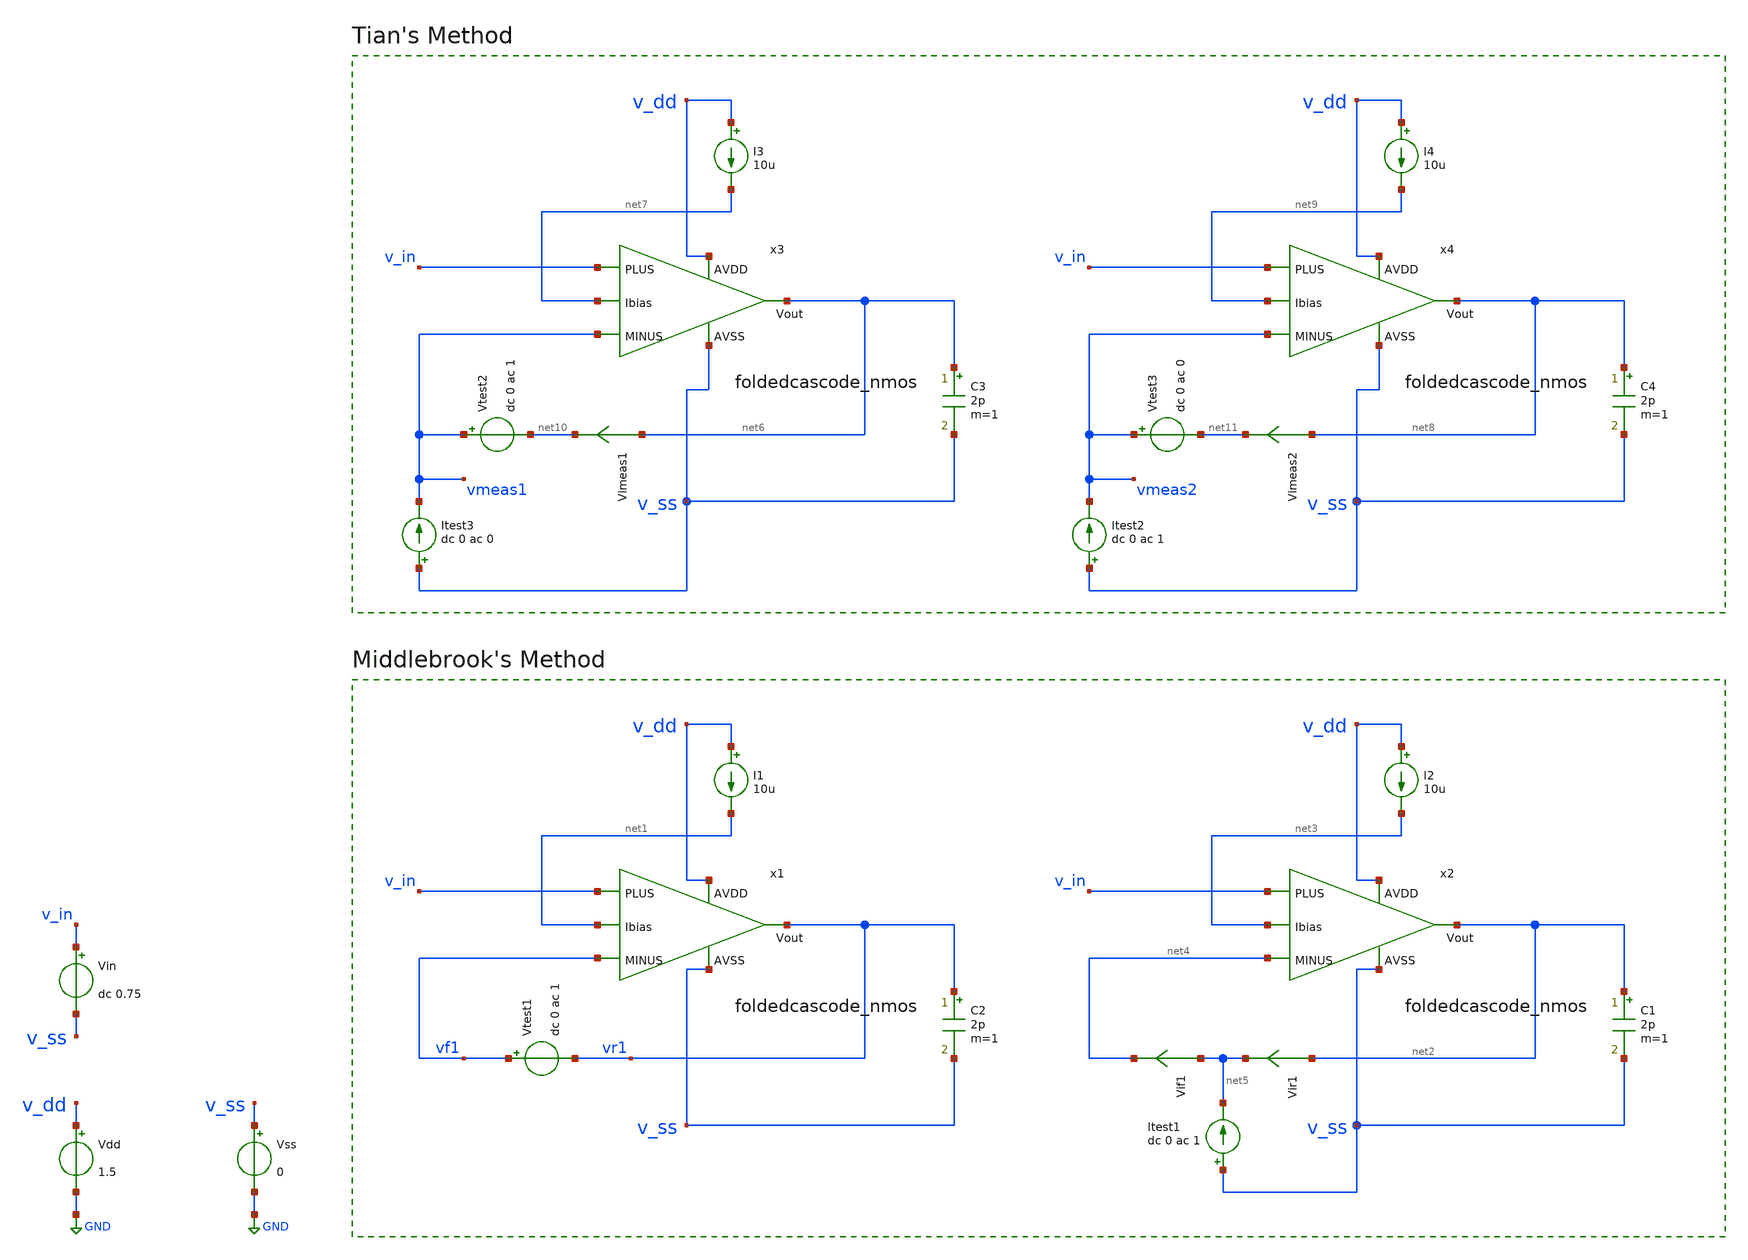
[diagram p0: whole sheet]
** sch_path: Designs/otas/1_schematics/tb_foldedcascode_nmos_loopgain.sch
* (c) 2025 Thesis_HP, Apache-2.0 license
**.subckt tb_foldedcascode_nmos_loopgain
Vdd v_dd GND 1.5
Vss v_ss GND 0
Vin v_in v_ss dc 0.75
C2 vr1 v_ss 2p m=1
I1 v_dd net1 10u
Vtest1 vf1 vr1 dc 0 ac 1
C1 net2 v_ss 2p m=1
I2 v_dd net3 10u
Vir1 net2 net5 0
.save i(vir1)
Vif1 net5 net4 0
.save i(vif1)
Itest1 v_ss net5 dc 0 ac 1
C3 net6 v_ss 2p m=1
I3 v_dd net7 10u
C4 net8 v_ss 2p m=1
I4 v_dd net9 10u
Itest3 v_ss vmeas1 dc 0 ac 0
Vtest2 vmeas1 net10 dc 0 ac 1
Vimeas1 net6 net10 0
.save i(vimeas1)
Itest2 v_ss vmeas2 dc 0 ac 1
Vtest3 vmeas2 net11 dc 0 ac 0
Vimeas2 net8 net11 0
.save i(vimeas2)
x3 v_dd v_in vmeas1 net6 net7 v_ss foldedcascode_nmos
x4 v_dd v_in vmeas2 net8 net9 v_ss foldedcascode_nmos
x1 v_dd v_in vf1 vr1 net1 v_ss foldedcascode_nmos
x2 v_dd v_in net4 net2 net3 v_ss foldedcascode_nmos
**** begin user architecture code

.lib cornerMOSlv.lib mos_tt
.lib cornerRES.lib res_typ



.param temp=27
.options savecurrents reltol=1e-3 abstol=1e-12 gmin=1e-15
.control
save all

* Operating Point Analysis
op
remzerovec
write foldedcascode_nmos_tb-loopgain.raw
set appendwrite

* AC Analysis
ac dec 101 1 100G
remzerovec
write foldedcascode_nmos_tb-loopgain.raw
set appendwrite

* Middlebrook's Method
let tv=-v(vr1)/v(vf1)
let ti=-i(vir1)/i(vif1)
let tmb=(tv*ti - 1)/(tv + ti + 2)

plot db(tmb) ylabel 'Magnitude - Middlebrook'
plot 180/pi*cphase(tmb) ylabel 'Phase - Middlebrook'

* Tian's Method
* vtest=0, itest=1:
let A=i(Vimeas2)
let C=v(vmeas2)

* vtest=1, itest=0:
let B=i(Vimeas1)
let D=v(vmeas1)
let ttian=(A*D-B*C-A)/(2*(B*C-A*D)+A-D+1)

plot db(ttian) ylabel 'Magnitude - Tian'
plot 180/pi*cphase(ttian) ylabel 'Phase - Tian'

* Middlebrook vs. Tian
plot db(tmb) db(ttian) ylabel 'Magnitude'
plot 180/pi*cphase(tmb) 180/pi*cphase(ttian) ylabel 'Phase'

write foldedcascode_nmos_tb-loopgain.raw

*quit
.endc


**** end user architecture code
**.ends

* expanding   symbol:  foldedcascode_nmos.sym # of pins=6
** sym_path: Designs/otas/foldedcascode_nmos.sym
** sch_path: Designs/otas/foldedcascode_nmos.sch
.subckt foldedcascode_nmos AVDD PLUS MINUS Vout Ibias AVSS
*.ipin PLUS
*.ipin MINUS
*.opin Vout
*.ipin AVDD
*.ipin AVSS
*.ipin Ibias
XM6 net5 PLUS net1 AVSS sg13_lv_nmos w=5u l=1u ng=1 m=1 mm_ok=1
XM8 net1 Ibias AVSS AVSS sg13_lv_nmos w=25u l=5u ng=3 m=1 mm_ok=1
XM21 net3 net4 AVSS AVSS sg13_lv_nmos w=1u l=0.5u ng=1 m=1 mm_ok=1
XM22 net2 net4 AVSS AVSS sg13_lv_nmos w=1u l=0.5u ng=1 m=1 mm_ok=1
XM7 net6 MINUS net1 AVSS sg13_lv_nmos w=5u l=1u ng=1 m=1 mm_ok=1
XM23 net4 net9 net2 AVSS sg13_lv_nmos w=1.5u l=0.5u ng=1 m=1 mm_ok=1
XM24 Vout net9 net3 AVSS sg13_lv_nmos w=1.5u l=0.5u ng=1 m=1 mm_ok=1
XM25 net4 net8 net5 AVDD sg13_lv_pmos w=6u l=0.5u ng=1 m=1 mm_ok=1
XM26 net5 net7 AVDD AVDD sg13_lv_pmos w=6u l=0.5u ng=1 m=1 mm_ok=1
XM27 Vout net8 net6 AVDD sg13_lv_pmos w=6u l=0.5u ng=1 m=1 mm_ok=1
XM28 net6 net7 AVDD AVDD sg13_lv_pmos w=6u l=0.5u ng=1 m=1 mm_ok=1
XM1 Ibias Ibias AVSS AVSS sg13_lv_nmos w=18u l=5u ng=2 m=1 mm_ok=1
XM2 net8 net8 net7 AVDD sg13_lv_pmos w=6u l=0.5u ng=2 m=1 mm_ok=1
XM3 net7 net7 AVDD AVDD sg13_lv_pmos w=6u l=0.5u ng=2 m=1 mm_ok=1
XM4 net9 net7 AVDD AVDD sg13_lv_pmos w=6u l=0.5u ng=2 m=1 mm_ok=1
XM5 net9 net9 AVSS AVSS sg13_lv_nmos w=1.5u l=0.5u ng=1 m=1 mm_ok=1
XM9 net8 Ibias AVSS AVSS sg13_lv_nmos w=25u l=5u ng=3 m=1 mm_ok=1
.ends

.GLOBAL GND
.end
